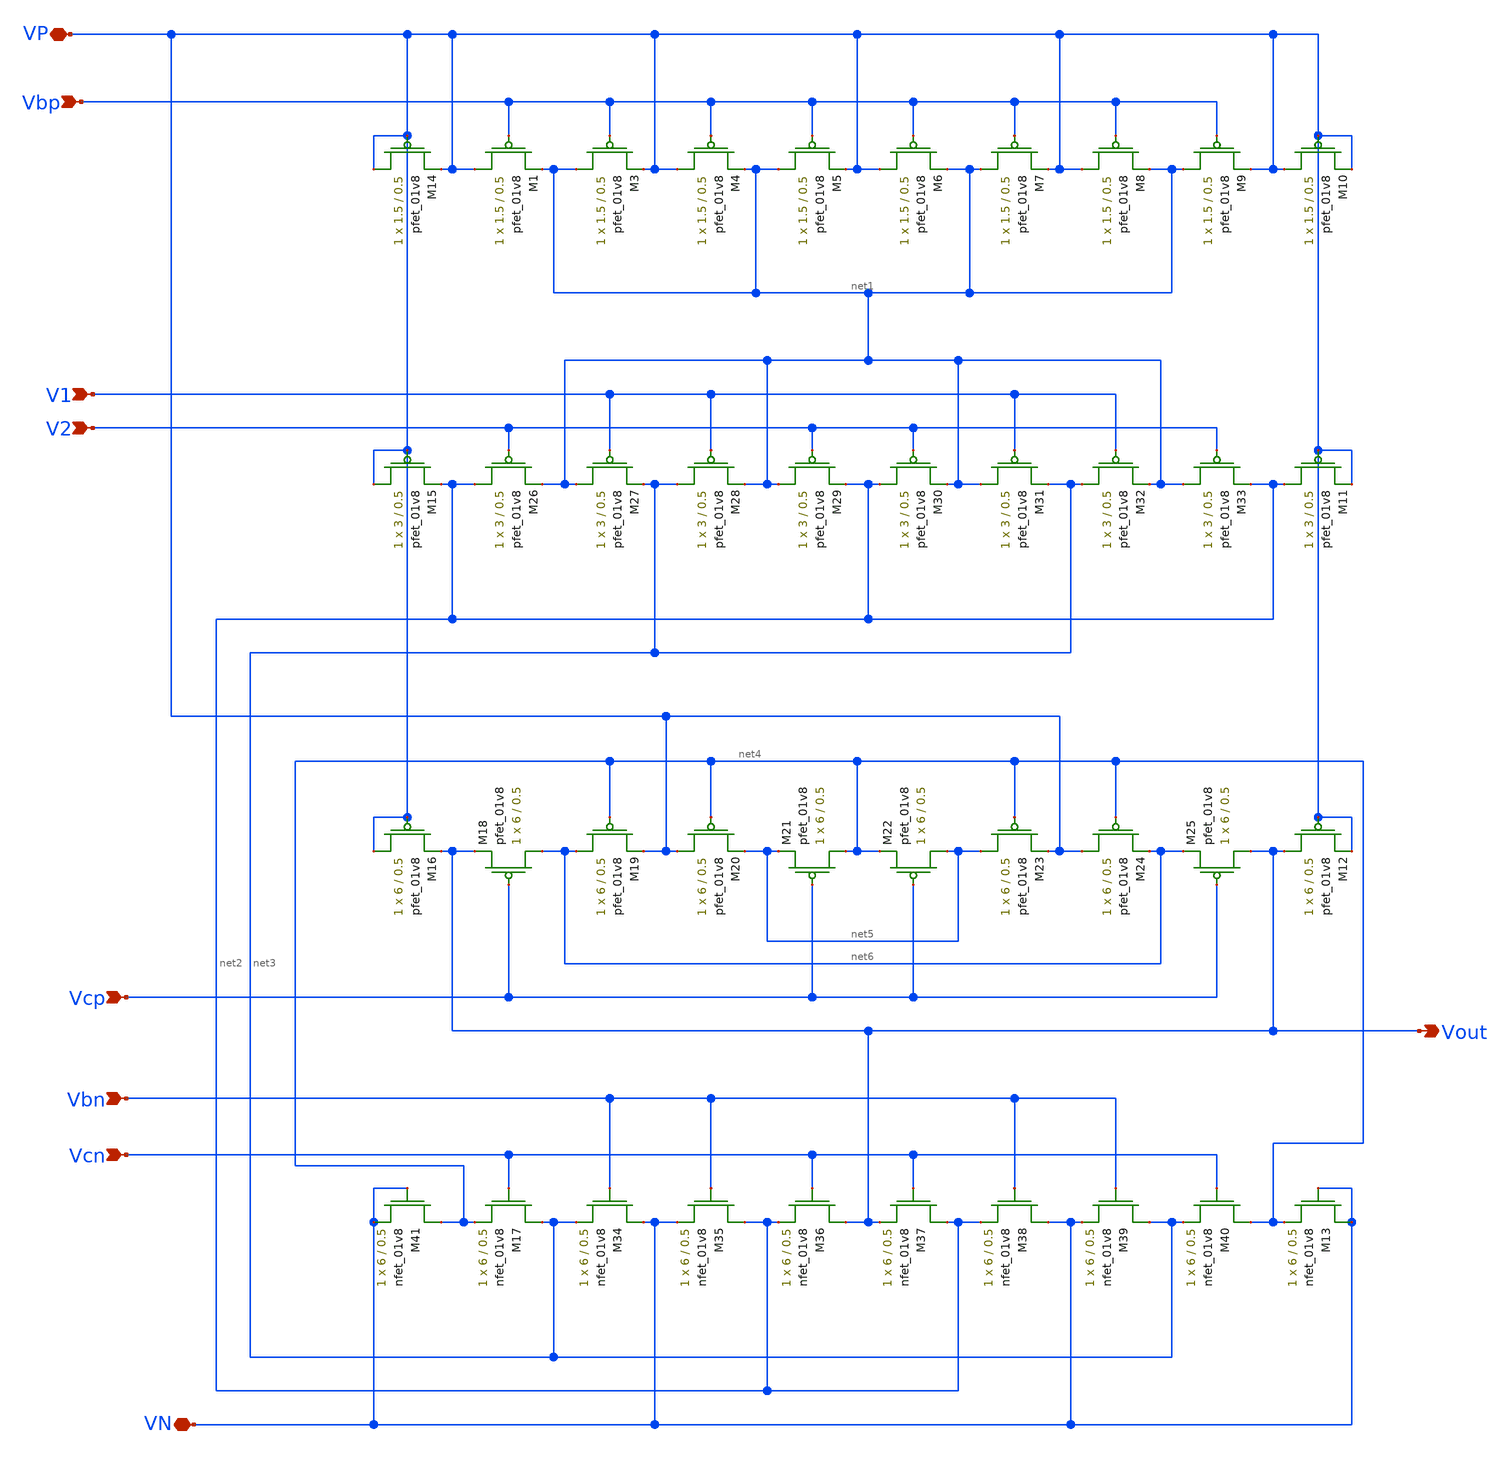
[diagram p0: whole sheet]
** sch_path: MP3/cascode-lds.sch
**.subckt cascode-lds VP VN Vbp V2 V1 Vcp Vbn Vcn Vout
*.iopin VP
*.iopin VN
*.ipin Vbp
*.ipin V2
*.ipin V1
*.ipin Vcp
*.ipin Vbn
*.ipin Vcn
*.opin Vout
XM1 VP Vbp net1 VDD sky130_fd_pr__pfet_01v8 L=0.5 W=1.5 nf=1 ad='int((nf+1)/2) * W/nf * 0.29' as='int((nf+2)/2) * W/nf * 0.29'
+ pd='2*int((nf+1)/2) * (W/nf + 0.29)' ps='2*int((nf+2)/2) * (W/nf + 0.29)' nrd='0.29 / W' nrs='0.29 / W'
+ sa=0 sb=0 sd=0 mult=1 m=1
XM3 net1 Vbp VP VDD sky130_fd_pr__pfet_01v8 L=0.5 W=1.5 nf=1 ad='int((nf+1)/2) * W/nf * 0.29' as='int((nf+2)/2) * W/nf * 0.29'
+ pd='2*int((nf+1)/2) * (W/nf + 0.29)' ps='2*int((nf+2)/2) * (W/nf + 0.29)' nrd='0.29 / W' nrs='0.29 / W'
+ sa=0 sb=0 sd=0 mult=1 m=1
XM4 VP Vbp net1 VDD sky130_fd_pr__pfet_01v8 L=0.5 W=1.5 nf=1 ad='int((nf+1)/2) * W/nf * 0.29' as='int((nf+2)/2) * W/nf * 0.29'
+ pd='2*int((nf+1)/2) * (W/nf + 0.29)' ps='2*int((nf+2)/2) * (W/nf + 0.29)' nrd='0.29 / W' nrs='0.29 / W'
+ sa=0 sb=0 sd=0 mult=1 m=1
XM5 net1 Vbp VP VDD sky130_fd_pr__pfet_01v8 L=0.5 W=1.5 nf=1 ad='int((nf+1)/2) * W/nf * 0.29' as='int((nf+2)/2) * W/nf * 0.29'
+ pd='2*int((nf+1)/2) * (W/nf + 0.29)' ps='2*int((nf+2)/2) * (W/nf + 0.29)' nrd='0.29 / W' nrs='0.29 / W'
+ sa=0 sb=0 sd=0 mult=1 m=1
XM6 VP Vbp net1 VDD sky130_fd_pr__pfet_01v8 L=0.5 W=1.5 nf=1 ad='int((nf+1)/2) * W/nf * 0.29' as='int((nf+2)/2) * W/nf * 0.29'
+ pd='2*int((nf+1)/2) * (W/nf + 0.29)' ps='2*int((nf+2)/2) * (W/nf + 0.29)' nrd='0.29 / W' nrs='0.29 / W'
+ sa=0 sb=0 sd=0 mult=1 m=1
XM7 net1 Vbp VP VDD sky130_fd_pr__pfet_01v8 L=0.5 W=1.5 nf=1 ad='int((nf+1)/2) * W/nf * 0.29' as='int((nf+2)/2) * W/nf * 0.29'
+ pd='2*int((nf+1)/2) * (W/nf + 0.29)' ps='2*int((nf+2)/2) * (W/nf + 0.29)' nrd='0.29 / W' nrs='0.29 / W'
+ sa=0 sb=0 sd=0 mult=1 m=1
XM8 VP Vbp net1 VDD sky130_fd_pr__pfet_01v8 L=0.5 W=1.5 nf=1 ad='int((nf+1)/2) * W/nf * 0.29' as='int((nf+2)/2) * W/nf * 0.29'
+ pd='2*int((nf+1)/2) * (W/nf + 0.29)' ps='2*int((nf+2)/2) * (W/nf + 0.29)' nrd='0.29 / W' nrs='0.29 / W'
+ sa=0 sb=0 sd=0 mult=1 m=1
XM9 net1 Vbp VP VDD sky130_fd_pr__pfet_01v8 L=0.5 W=1.5 nf=1 ad='int((nf+1)/2) * W/nf * 0.29' as='int((nf+2)/2) * W/nf * 0.29'
+ pd='2*int((nf+1)/2) * (W/nf + 0.29)' ps='2*int((nf+2)/2) * (W/nf + 0.29)' nrd='0.29 / W' nrs='0.29 / W'
+ sa=0 sb=0 sd=0 mult=1 m=1
XM18 net6 Vcp Vout VDD sky130_fd_pr__pfet_01v8 L=0.5 W=6 nf=1 ad='int((nf+1)/2) * W/nf * 0.29' as='int((nf+2)/2) * W/nf * 0.29'
+ pd='2*int((nf+1)/2) * (W/nf + 0.29)' ps='2*int((nf+2)/2) * (W/nf + 0.29)' nrd='0.29 / W' nrs='0.29 / W'
+ sa=0 sb=0 sd=0 mult=1 m=1
XM19 net6 net4 VP VDD sky130_fd_pr__pfet_01v8 L=0.5 W=6 nf=1 ad='int((nf+1)/2) * W/nf * 0.29' as='int((nf+2)/2) * W/nf * 0.29'
+ pd='2*int((nf+1)/2) * (W/nf + 0.29)' ps='2*int((nf+2)/2) * (W/nf + 0.29)' nrd='0.29 / W' nrs='0.29 / W'
+ sa=0 sb=0 sd=0 mult=1 m=1
XM20 VP net4 net5 VDD sky130_fd_pr__pfet_01v8 L=0.5 W=6 nf=1 ad='int((nf+1)/2) * W/nf * 0.29' as='int((nf+2)/2) * W/nf * 0.29'
+ pd='2*int((nf+1)/2) * (W/nf + 0.29)' ps='2*int((nf+2)/2) * (W/nf + 0.29)' nrd='0.29 / W' nrs='0.29 / W'
+ sa=0 sb=0 sd=0 mult=1 m=1
XM21 net4 Vcp net5 VDD sky130_fd_pr__pfet_01v8 L=0.5 W=6 nf=1 ad='int((nf+1)/2) * W/nf * 0.29' as='int((nf+2)/2) * W/nf * 0.29'
+ pd='2*int((nf+1)/2) * (W/nf + 0.29)' ps='2*int((nf+2)/2) * (W/nf + 0.29)' nrd='0.29 / W' nrs='0.29 / W'
+ sa=0 sb=0 sd=0 mult=1 m=1
XM22 net5 Vcp net4 VDD sky130_fd_pr__pfet_01v8 L=0.5 W=6 nf=1 ad='int((nf+1)/2) * W/nf * 0.29' as='int((nf+2)/2) * W/nf * 0.29'
+ pd='2*int((nf+1)/2) * (W/nf + 0.29)' ps='2*int((nf+2)/2) * (W/nf + 0.29)' nrd='0.29 / W' nrs='0.29 / W'
+ sa=0 sb=0 sd=0 mult=1 m=1
XM23 net5 net4 VP VDD sky130_fd_pr__pfet_01v8 L=0.5 W=6 nf=1 ad='int((nf+1)/2) * W/nf * 0.29' as='int((nf+2)/2) * W/nf * 0.29'
+ pd='2*int((nf+1)/2) * (W/nf + 0.29)' ps='2*int((nf+2)/2) * (W/nf + 0.29)' nrd='0.29 / W' nrs='0.29 / W'
+ sa=0 sb=0 sd=0 mult=1 m=1
XM24 VP net4 net6 VDD sky130_fd_pr__pfet_01v8 L=0.5 W=6 nf=1 ad='int((nf+1)/2) * W/nf * 0.29' as='int((nf+2)/2) * W/nf * 0.29'
+ pd='2*int((nf+1)/2) * (W/nf + 0.29)' ps='2*int((nf+2)/2) * (W/nf + 0.29)' nrd='0.29 / W' nrs='0.29 / W'
+ sa=0 sb=0 sd=0 mult=1 m=1
XM25 Vout Vcp net6 VDD sky130_fd_pr__pfet_01v8 L=0.5 W=6 nf=1 ad='int((nf+1)/2) * W/nf * 0.29' as='int((nf+2)/2) * W/nf * 0.29'
+ pd='2*int((nf+1)/2) * (W/nf + 0.29)' ps='2*int((nf+2)/2) * (W/nf + 0.29)' nrd='0.29 / W' nrs='0.29 / W'
+ sa=0 sb=0 sd=0 mult=1 m=1
XM26 net2 V2 net1 VDD sky130_fd_pr__pfet_01v8 L=0.5 W=3 nf=1 ad='int((nf+1)/2) * W/nf * 0.29' as='int((nf+2)/2) * W/nf * 0.29'
+ pd='2*int((nf+1)/2) * (W/nf + 0.29)' ps='2*int((nf+2)/2) * (W/nf + 0.29)' nrd='0.29 / W' nrs='0.29 / W'
+ sa=0 sb=0 sd=0 mult=1 m=1
XM27 net1 V1 net3 VDD sky130_fd_pr__pfet_01v8 L=0.5 W=3 nf=1 ad='int((nf+1)/2) * W/nf * 0.29' as='int((nf+2)/2) * W/nf * 0.29'
+ pd='2*int((nf+1)/2) * (W/nf + 0.29)' ps='2*int((nf+2)/2) * (W/nf + 0.29)' nrd='0.29 / W' nrs='0.29 / W'
+ sa=0 sb=0 sd=0 mult=1 m=1
XM28 net3 V1 net1 VDD sky130_fd_pr__pfet_01v8 L=0.5 W=3 nf=1 ad='int((nf+1)/2) * W/nf * 0.29' as='int((nf+2)/2) * W/nf * 0.29'
+ pd='2*int((nf+1)/2) * (W/nf + 0.29)' ps='2*int((nf+2)/2) * (W/nf + 0.29)' nrd='0.29 / W' nrs='0.29 / W'
+ sa=0 sb=0 sd=0 mult=1 m=1
XM29 net1 V2 net2 VDD sky130_fd_pr__pfet_01v8 L=0.5 W=3 nf=1 ad='int((nf+1)/2) * W/nf * 0.29' as='int((nf+2)/2) * W/nf * 0.29'
+ pd='2*int((nf+1)/2) * (W/nf + 0.29)' ps='2*int((nf+2)/2) * (W/nf + 0.29)' nrd='0.29 / W' nrs='0.29 / W'
+ sa=0 sb=0 sd=0 mult=1 m=1
XM30 net2 V2 net1 VDD sky130_fd_pr__pfet_01v8 L=0.5 W=3 nf=1 ad='int((nf+1)/2) * W/nf * 0.29' as='int((nf+2)/2) * W/nf * 0.29'
+ pd='2*int((nf+1)/2) * (W/nf + 0.29)' ps='2*int((nf+2)/2) * (W/nf + 0.29)' nrd='0.29 / W' nrs='0.29 / W'
+ sa=0 sb=0 sd=0 mult=1 m=1
XM31 net1 V1 net3 VDD sky130_fd_pr__pfet_01v8 L=0.5 W=3 nf=1 ad='int((nf+1)/2) * W/nf * 0.29' as='int((nf+2)/2) * W/nf * 0.29'
+ pd='2*int((nf+1)/2) * (W/nf + 0.29)' ps='2*int((nf+2)/2) * (W/nf + 0.29)' nrd='0.29 / W' nrs='0.29 / W'
+ sa=0 sb=0 sd=0 mult=1 m=1
XM32 net3 V1 net1 VDD sky130_fd_pr__pfet_01v8 L=0.5 W=3 nf=1 ad='int((nf+1)/2) * W/nf * 0.29' as='int((nf+2)/2) * W/nf * 0.29'
+ pd='2*int((nf+1)/2) * (W/nf + 0.29)' ps='2*int((nf+2)/2) * (W/nf + 0.29)' nrd='0.29 / W' nrs='0.29 / W'
+ sa=0 sb=0 sd=0 mult=1 m=1
XM33 net1 V2 net2 VDD sky130_fd_pr__pfet_01v8 L=0.5 W=3 nf=1 ad='int((nf+1)/2) * W/nf * 0.29' as='int((nf+2)/2) * W/nf * 0.29'
+ pd='2*int((nf+1)/2) * (W/nf + 0.29)' ps='2*int((nf+2)/2) * (W/nf + 0.29)' nrd='0.29 / W' nrs='0.29 / W'
+ sa=0 sb=0 sd=0 mult=1 m=1
XM34 VN Vbn net3 GND sky130_fd_pr__nfet_01v8 L=0.5 W=6 nf=1 ad='int((nf+1)/2) * W/nf * 0.29' as='int((nf+2)/2) * W/nf * 0.29'
+ pd='2*int((nf+1)/2) * (W/nf + 0.29)' ps='2*int((nf+2)/2) * (W/nf + 0.29)' nrd='0.29 / W' nrs='0.29 / W'
+ sa=0 sb=0 sd=0 mult=1 m=1
XM35 net2 Vbn VN GND sky130_fd_pr__nfet_01v8 L=0.5 W=6 nf=1 ad='int((nf+1)/2) * W/nf * 0.29' as='int((nf+2)/2) * W/nf * 0.29'
+ pd='2*int((nf+1)/2) * (W/nf + 0.29)' ps='2*int((nf+2)/2) * (W/nf + 0.29)' nrd='0.29 / W' nrs='0.29 / W'
+ sa=0 sb=0 sd=0 mult=1 m=1
XM36 Vout Vcn net2 GND sky130_fd_pr__nfet_01v8 L=0.5 W=6 nf=1 ad='int((nf+1)/2) * W/nf * 0.29' as='int((nf+2)/2) * W/nf * 0.29'
+ pd='2*int((nf+1)/2) * (W/nf + 0.29)' ps='2*int((nf+2)/2) * (W/nf + 0.29)' nrd='0.29 / W' nrs='0.29 / W'
+ sa=0 sb=0 sd=0 mult=1 m=1
XM37 net2 Vcn Vout GND sky130_fd_pr__nfet_01v8 L=0.5 W=6 nf=1 ad='int((nf+1)/2) * W/nf * 0.29' as='int((nf+2)/2) * W/nf * 0.29'
+ pd='2*int((nf+1)/2) * (W/nf + 0.29)' ps='2*int((nf+2)/2) * (W/nf + 0.29)' nrd='0.29 / W' nrs='0.29 / W'
+ sa=0 sb=0 sd=0 mult=1 m=1
XM38 VN Vbn net2 GND sky130_fd_pr__nfet_01v8 L=0.5 W=6 nf=1 ad='int((nf+1)/2) * W/nf * 0.29' as='int((nf+2)/2) * W/nf * 0.29'
+ pd='2*int((nf+1)/2) * (W/nf + 0.29)' ps='2*int((nf+2)/2) * (W/nf + 0.29)' nrd='0.29 / W' nrs='0.29 / W'
+ sa=0 sb=0 sd=0 mult=1 m=1
XM39 net3 Vbn VN GND sky130_fd_pr__nfet_01v8 L=0.5 W=6 nf=1 ad='int((nf+1)/2) * W/nf * 0.29' as='int((nf+2)/2) * W/nf * 0.29'
+ pd='2*int((nf+1)/2) * (W/nf + 0.29)' ps='2*int((nf+2)/2) * (W/nf + 0.29)' nrd='0.29 / W' nrs='0.29 / W'
+ sa=0 sb=0 sd=0 mult=1 m=1
XM40 net4 Vcn net3 GND sky130_fd_pr__nfet_01v8 L=0.5 W=6 nf=1 ad='int((nf+1)/2) * W/nf * 0.29' as='int((nf+2)/2) * W/nf * 0.29'
+ pd='2*int((nf+1)/2) * (W/nf + 0.29)' ps='2*int((nf+2)/2) * (W/nf + 0.29)' nrd='0.29 / W' nrs='0.29 / W'
+ sa=0 sb=0 sd=0 mult=1 m=1
XM10 VP VP VP VDD sky130_fd_pr__pfet_01v8 L=0.5 W=1.5 nf=1 ad='int((nf+1)/2) * W/nf * 0.29' as='int((nf+2)/2) * W/nf * 0.29'
+ pd='2*int((nf+1)/2) * (W/nf + 0.29)' ps='2*int((nf+2)/2) * (W/nf + 0.29)' nrd='0.29 / W' nrs='0.29 / W'
+ sa=0 sb=0 sd=0 mult=1 m=1
XM11 net2 VP VP VDD sky130_fd_pr__pfet_01v8 L=0.5 W=3 nf=1 ad='int((nf+1)/2) * W/nf * 0.29' as='int((nf+2)/2) * W/nf * 0.29'
+ pd='2*int((nf+1)/2) * (W/nf + 0.29)' ps='2*int((nf+2)/2) * (W/nf + 0.29)' nrd='0.29 / W' nrs='0.29 / W'
+ sa=0 sb=0 sd=0 mult=1 m=1
XM12 Vout VP VP VDD sky130_fd_pr__pfet_01v8 L=0.5 W=6 nf=1 ad='int((nf+1)/2) * W/nf * 0.29' as='int((nf+2)/2) * W/nf * 0.29'
+ pd='2*int((nf+1)/2) * (W/nf + 0.29)' ps='2*int((nf+2)/2) * (W/nf + 0.29)' nrd='0.29 / W' nrs='0.29 / W'
+ sa=0 sb=0 sd=0 mult=1 m=1
XM13 VN VN net4 GND sky130_fd_pr__nfet_01v8 L=0.5 W=6 nf=1 ad='int((nf+1)/2) * W/nf * 0.29' as='int((nf+2)/2) * W/nf * 0.29'
+ pd='2*int((nf+1)/2) * (W/nf + 0.29)' ps='2*int((nf+2)/2) * (W/nf + 0.29)' nrd='0.29 / W' nrs='0.29 / W'
+ sa=0 sb=0 sd=0 mult=1 m=1
XM14 VP VP VP VDD sky130_fd_pr__pfet_01v8 L=0.5 W=1.5 nf=1 ad='int((nf+1)/2) * W/nf * 0.29' as='int((nf+2)/2) * W/nf * 0.29'
+ pd='2*int((nf+1)/2) * (W/nf + 0.29)' ps='2*int((nf+2)/2) * (W/nf + 0.29)' nrd='0.29 / W' nrs='0.29 / W'
+ sa=0 sb=0 sd=0 mult=1 m=1
XM15 VP VP net2 VDD sky130_fd_pr__pfet_01v8 L=0.5 W=3 nf=1 ad='int((nf+1)/2) * W/nf * 0.29' as='int((nf+2)/2) * W/nf * 0.29'
+ pd='2*int((nf+1)/2) * (W/nf + 0.29)' ps='2*int((nf+2)/2) * (W/nf + 0.29)' nrd='0.29 / W' nrs='0.29 / W'
+ sa=0 sb=0 sd=0 mult=1 m=1
XM16 VP VP Vout VDD sky130_fd_pr__pfet_01v8 L=0.5 W=6 nf=1 ad='int((nf+1)/2) * W/nf * 0.29' as='int((nf+2)/2) * W/nf * 0.29'
+ pd='2*int((nf+1)/2) * (W/nf + 0.29)' ps='2*int((nf+2)/2) * (W/nf + 0.29)' nrd='0.29 / W' nrs='0.29 / W'
+ sa=0 sb=0 sd=0 mult=1 m=1
XM17 net3 Vcn net4 GND sky130_fd_pr__nfet_01v8 L=0.5 W=6 nf=1 ad='int((nf+1)/2) * W/nf * 0.29' as='int((nf+2)/2) * W/nf * 0.29'
+ pd='2*int((nf+1)/2) * (W/nf + 0.29)' ps='2*int((nf+2)/2) * (W/nf + 0.29)' nrd='0.29 / W' nrs='0.29 / W'
+ sa=0 sb=0 sd=0 mult=1 m=1
XM41 net4 VN VN GND sky130_fd_pr__nfet_01v8 L=0.5 W=6 nf=1 ad='int((nf+1)/2) * W/nf * 0.29' as='int((nf+2)/2) * W/nf * 0.29'
+ pd='2*int((nf+1)/2) * (W/nf + 0.29)' ps='2*int((nf+2)/2) * (W/nf + 0.29)' nrd='0.29 / W' nrs='0.29 / W'
+ sa=0 sb=0 sd=0 mult=1 m=1
**.ends
.end
